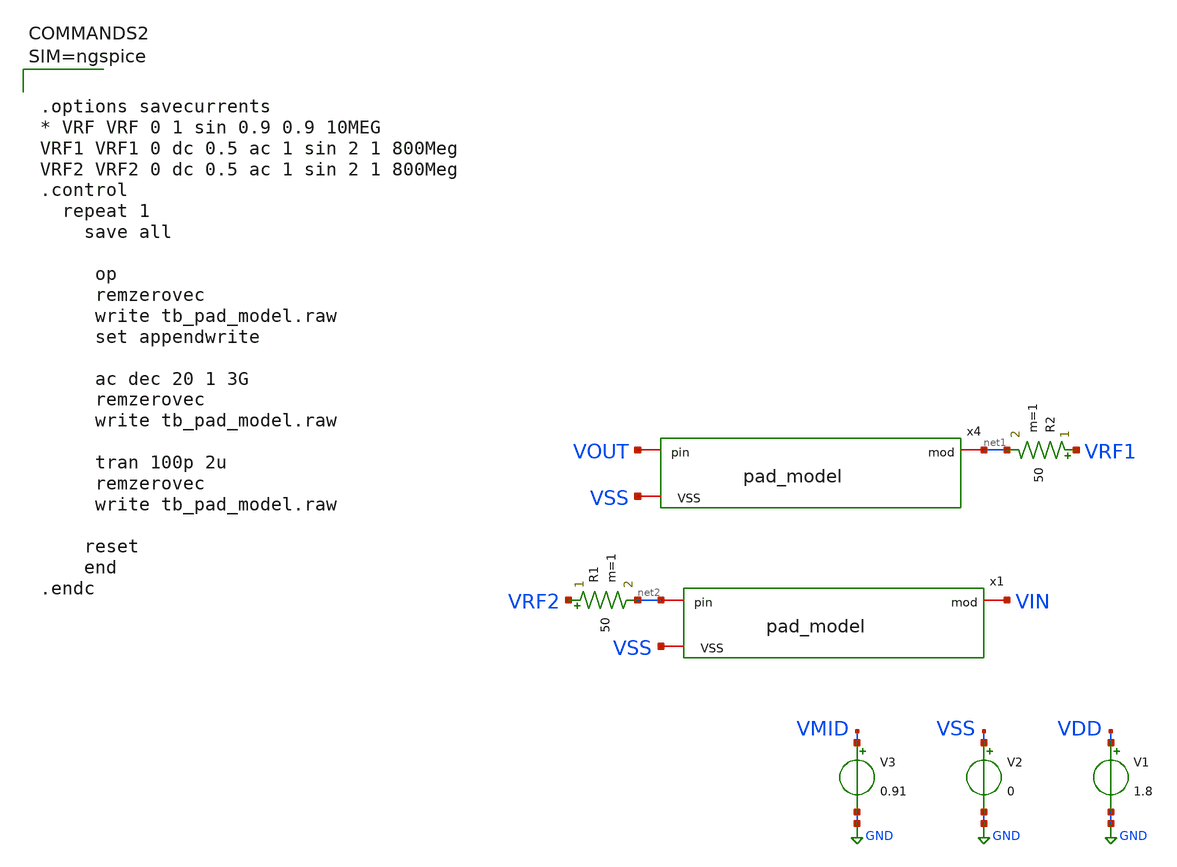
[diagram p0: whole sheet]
** sch_path: xschem/tb_pad_model.sch
**.subckt tb_pad_model
V1 VDD GND 1.8
V2 VSS GND 0
V3 VMID GND 0.91
x4 VSS VOUT net1 pad_model
R2 VRF1 net1 50 m=1
x1 VSS net2 VIN pad_model
R1 VRF2 net2 50 m=1
**** begin user architecture code

** opencircuitdesign pdks install
.lib $::SKYWATER_MODELS/sky130.lib.spice tt





.options savecurrents
* VRF VRF 0 1 sin 0.9 0.9 10MEG
VRF1 VRF1 0 dc 0.5 ac 1 sin 2 1 800Meg
VRF2 VRF2 0 dc 0.5 ac 1 sin 2 1 800Meg
.control
  repeat 1
    save all

     op
     remzerovec
     write tb_pad_model.raw
     set appendwrite

     ac dec 20 1 3G
     remzerovec
     write tb_pad_model.raw

     tran 100p 2u
     remzerovec
     write tb_pad_model.raw

    reset
    end
.endc



**** end user architecture code
**.ends

* expanding   symbol:  pad_model.sym # of pins=3
** sym_path: xschem/pad_model.sym
** sch_path: xschem/pad_model.sch
.subckt pad_model VSS pin mod
*.iopin pin
*.iopin mod
*.iopin VSS
XM1 net3 VAPWR mod VSS sky130_fd_pr__nfet_g5v0d10v5 L=0.5 W=60 nf=12 ad='int((nf+1)/2) * W/nf * 0.29'
+ as='int((nf+2)/2) * W/nf * 0.29' pd='2*int((nf+1)/2) * (W/nf + 0.29)' ps='2*int((nf+2)/2) * (W/nf + 0.29)'
+ nrd='0.29 / W' nrs='0.29 / W' sa=0 sb=0 sd=0 mult=1 m=1
XM2 net3 VSS mod VAPWR sky130_fd_pr__pfet_g5v0d10v5 L=0.5 W=180 nf=18 ad='int((nf+1)/2) * W/nf * 0.29'
+ as='int((nf+2)/2) * W/nf * 0.29' pd='2*int((nf+1)/2) * (W/nf + 0.29)' ps='2*int((nf+2)/2) * (W/nf + 0.29)'
+ nrd='0.29 / W' nrs='0.29 / W' sa=0 sb=0 sd=0 mult=1 m=1
C1 pin VSS 2p m=1
V1 VAPWR VSS 3.3
R1 net1 pin 1 m=1
L1 net2 net1 1n m=1
C2 net2 VSS 3p m=1
R2 net3 net2 50 m=1
C3 mod VSS 250f m=1
XM3 net3 VSS VSS VSS sky130_fd_pr__nfet_g5v0d10v5 L=0.5 W=60 nf=12 ad='int((nf+1)/2) * W/nf * 0.29' as='int((nf+2)/2) * W/nf * 0.29'
+ pd='2*int((nf+1)/2) * (W/nf + 0.29)' ps='2*int((nf+2)/2) * (W/nf + 0.29)' nrd='0.29 / W' nrs='0.29 / W'
+ sa=0 sb=0 sd=0 mult=15 m=15
XM4 net3 VAPWR VSS VAPWR sky130_fd_pr__pfet_g5v0d10v5 L=0.5 W=180 nf=18 ad='int((nf+1)/2) * W/nf * 0.29'
+ as='int((nf+2)/2) * W/nf * 0.29' pd='2*int((nf+1)/2) * (W/nf + 0.29)' ps='2*int((nf+2)/2) * (W/nf + 0.29)'
+ nrd='0.29 / W' nrs='0.29 / W' sa=0 sb=0 sd=0 mult=15 m=15
.ends

.GLOBAL GND
.end
